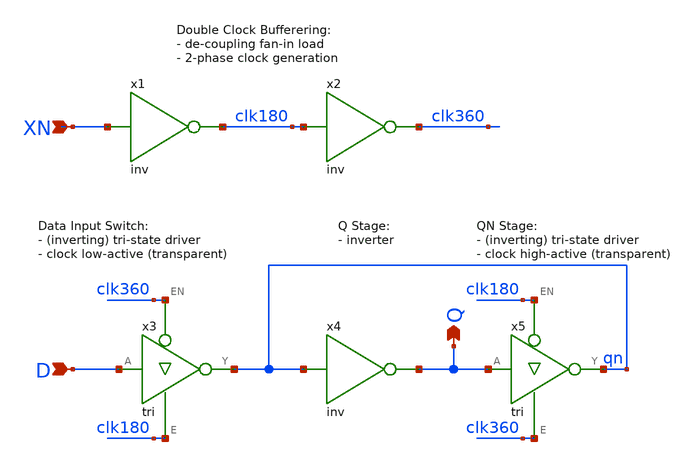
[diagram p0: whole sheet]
** sch_path: Sources/crafted/LATN.sch
**.subckt LATN XN D Q
*.ipin XN
*.ipin D
*.opin Q
x1 XN clk180 VDD GND inv Wmin=1.5u Lmin=1u g=2 m=1
x2 clk180 clk360 VDD GND inv Wmin=1.5u Lmin=1u g=2 m=1
x4 qn Q VDD GND inv Wmin=1.5u Lmin=1u g=2 m=1
x3 D clk360 clk180 qn VDD GND tri Wmin=1.5u Lmin=1u g=2 m=1
x5 Q clk180 clk360 qn VDD GND tri Wmin=1.5u Lmin=1u g=2 m=1
**.ends

* expanding   symbol:  inv.sym # of pins=2
** sym_path: Sources/crafted/inv.sym
** sch_path: Sources/crafted/inv.sch
.subckt inv A Y VDD GND    Wmin=1.5u Lmin=1u g=2
*.ipin A
*.opin Y
m2 Y A GND GND nmos4 w=Wmin l=Lmin m=m
m1 Y A VDD VDD pmos4 w='g*Wmin' l=Lmin m=m
.ends


* expanding   symbol:  tri.sym # of pins=4
** sym_path: Sources/crafted/tri.sym
** sch_path: Sources/crafted/tri.sch
.subckt tri A EN E Y VDD GND    Wmin=1.5u Lmin=1u g=2
*.ipin A
*.iopin Y
*.ipin EN
*.ipin E
m2 Y A net2 GND nmos4 w='2*Wmin' l=Lmin m=m
m1 Y A net1 VDD pmos4 w='2*g*Wmin' l=Lmin m=m
m0 net2 E GND GND nmos4 w='2*Wmin' l=Lmin m=m
m3 net1 EN VDD VDD pmos4 w='2*g*Wmin' l=Lmin m=m
.ends

.GLOBAL VDD
.GLOBAL GND
.end
